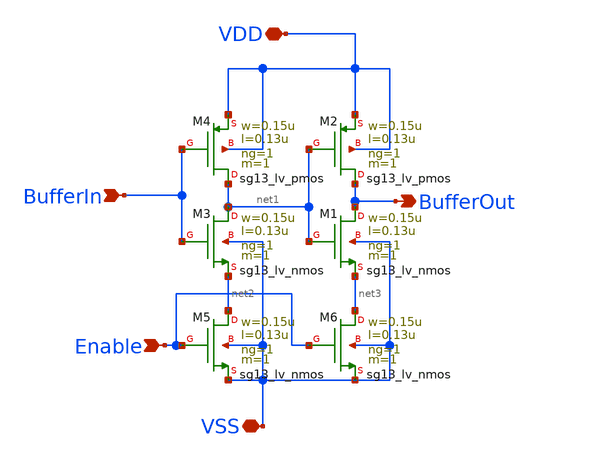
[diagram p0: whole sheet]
** sch_path: circuit_files/sar_adc_20260903/hiZEnableSwitch.sch
**.subckt hiZEnableSwitch BufferIn BufferOut VDD VSS Enable
*.ipin BufferIn
*.opin BufferOut
*.iopin VDD
*.iopin VSS
*.ipin Enable
XM1 BufferOut net1 net3 VSS sg13_lv_nmos w=0.15u l=0.13u ng=1 m=1 mm_ok=1
XM2 BufferOut net1 VDD VDD sg13_lv_pmos w=0.15u l=0.13u ng=1 m=1 mm_ok=1
XM3 net1 BufferIn net2 VSS sg13_lv_nmos w=0.15u l=0.13u ng=1 m=1 mm_ok=1
XM4 net1 BufferIn VDD VDD sg13_lv_pmos w=0.15u l=0.13u ng=1 m=1 mm_ok=1
XM5 net2 Enable VSS VSS sg13_lv_nmos w=0.15u l=0.13u ng=1 m=1 mm_ok=1
XM6 net3 Enable VSS VSS sg13_lv_nmos w=0.15u l=0.13u ng=1 m=1 mm_ok=1
**.ends
.end
